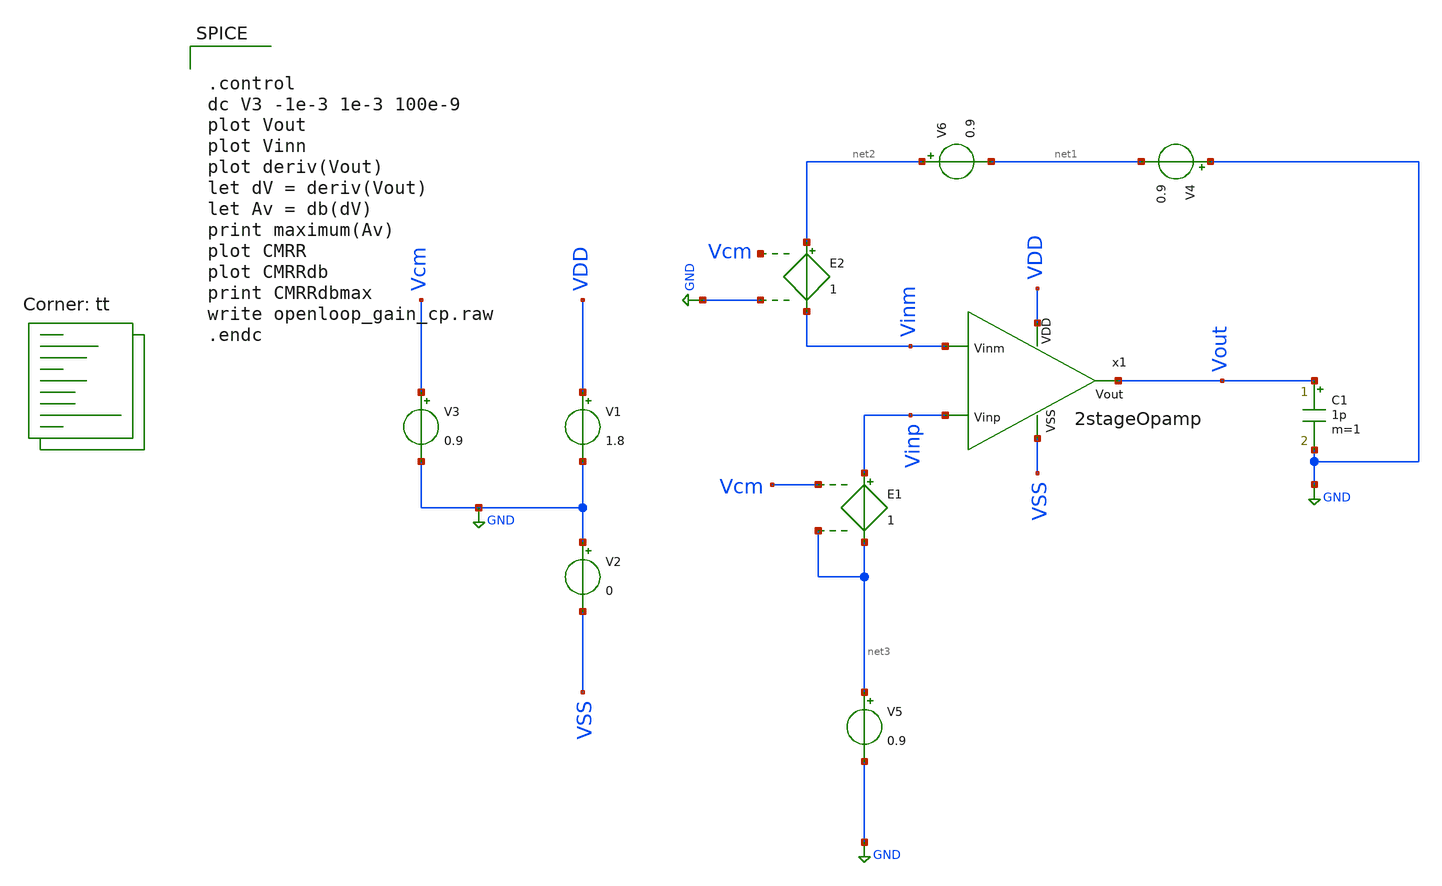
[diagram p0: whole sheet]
** sch_path: xschem/test/xschem/dec24_2stage_tbs/openloop_gain_cp.sch
**.subckt openloop_gain_cp
V1 VDD GND 1.8
V2 GND VSS 0
V3 Vcm GND 0.9
x1 VDD Vinm Vinp Vout VSS 2stageOpamp
E1 Vinp net3 Vcm net3 1
E2 net2 Vinm Vcm GND 1
V4 GND net1 0.9
C1 Vout GND 1p m=1
V5 net3 GND 0.9
V6 net2 net1 0.9
**** begin user architecture code


.control
dc V3 -1e-3 1e-3 100e-9
plot Vout
plot Vinn
plot deriv(Vout)
let dV = deriv(Vout)
let Av = db(dV)
print maximum(Av)
plot CMRR
plot CMRRdb
print CMRRdbmax
write openloop_gain_cp.raw
.endc



.lib $::SKYWATER_MODELS/sky130.lib.spice tt
**** end user architecture code
**.ends

* expanding   symbol:  amplifiers/dec24/2stageOpamp.sym # of pins=5
** sym_path: amplifiers/dec24/2stageOpamp.sym
** sch_path: amplifiers/dec24/2stageOpamp.sch
.subckt 2stageOpamp VDD Vinm Vinp Vout VSS
*.ipin Vinm
*.ipin Vinp
*.opin Vout
*.ipin VSS
*.ipin VDD
XM8 Vout net1 VSS VSS sky130_fd_pr__nfet_01v8 L=1 W=6 nf=1 ad='int((nf+1)/2) * W/nf * 0.29' as='int((nf+2)/2) * W/nf * 0.29'
+ pd='2*int((nf+1)/2) * (W/nf + 0.29)' ps='2*int((nf+2)/2) * (W/nf + 0.29)' nrd='0.29 / W' nrs='0.29 / W'
+ sa=0 sb=0 sd=0 mult=8 m=8
XM2 Vout Vb1 VDD VDD sky130_fd_pr__pfet_01v8_lvt L=1 W=9 nf=1 ad='int((nf+1)/2) * W/nf * 0.29' as='int((nf+2)/2) * W/nf * 0.29'
+ pd='2*int((nf+1)/2) * (W/nf + 0.29)' ps='2*int((nf+2)/2) * (W/nf + 0.29)' nrd='0.29 / W' nrs='0.29 / W'
+ sa=0 sb=0 sd=0 mult=3 m=3
XM5 net5 Vb3 net6 VSS sky130_fd_pr__nfet_01v8 L=1 W=4 nf=1 ad='int((nf+1)/2) * W/nf * 0.29' as='int((nf+2)/2) * W/nf * 0.29'
+ pd='2*int((nf+1)/2) * (W/nf + 0.29)' ps='2*int((nf+2)/2) * (W/nf + 0.29)' nrd='0.29 / W' nrs='0.29 / W'
+ sa=0 sb=0 sd=0 mult=3 m=3
XM17 net1 Vb3 net7 VSS sky130_fd_pr__nfet_01v8 L=1 W=4 nf=1 ad='int((nf+1)/2) * W/nf * 0.29' as='int((nf+2)/2) * W/nf * 0.29'
+ pd='2*int((nf+1)/2) * (W/nf + 0.29)' ps='2*int((nf+2)/2) * (W/nf + 0.29)' nrd='0.29 / W' nrs='0.29 / W'
+ sa=0 sb=0 sd=0 mult=3 m=3
XM3 net6 net5 VSS VSS sky130_fd_pr__nfet_01v8 L=1 W=8 nf=1 ad='int((nf+1)/2) * W/nf * 0.29' as='int((nf+2)/2) * W/nf * 0.29'
+ pd='2*int((nf+1)/2) * (W/nf + 0.29)' ps='2*int((nf+2)/2) * (W/nf + 0.29)' nrd='0.29 / W' nrs='0.29 / W'
+ sa=0 sb=0 sd=0 mult=1 m=1
XM19 net7 net5 VSS VSS sky130_fd_pr__nfet_01v8 L=1 W=8 nf=1 ad='int((nf+1)/2) * W/nf * 0.29' as='int((nf+2)/2) * W/nf * 0.29'
+ pd='2*int((nf+1)/2) * (W/nf + 0.29)' ps='2*int((nf+2)/2) * (W/nf + 0.29)' nrd='0.29 / W' nrs='0.29 / W'
+ sa=0 sb=0 sd=0 mult=1 m=1
V1 Vb1 GND 1.1
V2 Vb2 GND 0.7
V3 Vb3 GND 0.9
XM11 net8 Vb1 VDD VDD sky130_fd_pr__pfet_01v8_lvt L=1 W=9 nf=1 ad='int((nf+1)/2) * W/nf * 0.29' as='int((nf+2)/2) * W/nf * 0.29'
+ pd='2*int((nf+1)/2) * (W/nf + 0.29)' ps='2*int((nf+2)/2) * (W/nf + 0.29)' nrd='0.29 / W' nrs='0.29 / W'
+ sa=0 sb=0 sd=0 mult=2 m=2
XM1 net6 Vinm net8 VDD sky130_fd_pr__pfet_01v8_lvt L=1 W=8 nf=1 ad='int((nf+1)/2) * W/nf * 0.29' as='int((nf+2)/2) * W/nf * 0.29'
+ pd='2*int((nf+1)/2) * (W/nf + 0.29)' ps='2*int((nf+2)/2) * (W/nf + 0.29)' nrd='0.29 / W' nrs='0.29 / W'
+ sa=0 sb=0 sd=0 mult=3 m=3
XM15 net7 Vinp net8 VDD sky130_fd_pr__pfet_01v8_lvt L=1 W=8 nf=1 ad='int((nf+1)/2) * W/nf * 0.29' as='int((nf+2)/2) * W/nf * 0.29'
+ pd='2*int((nf+1)/2) * (W/nf + 0.29)' ps='2*int((nf+2)/2) * (W/nf + 0.29)' nrd='0.29 / W' nrs='0.29 / W'
+ sa=0 sb=0 sd=0 mult=3 m=3
XM7 net3 Vb1 VDD VDD sky130_fd_pr__pfet_01v8_lvt L=1 W=9 nf=1 ad='int((nf+1)/2) * W/nf * 0.29' as='int((nf+2)/2) * W/nf * 0.29'
+ pd='2*int((nf+1)/2) * (W/nf + 0.29)' ps='2*int((nf+2)/2) * (W/nf + 0.29)' nrd='0.29 / W' nrs='0.29 / W'
+ sa=0 sb=0 sd=0 mult=1 m=1
XM21 net4 Vb1 VDD VDD sky130_fd_pr__pfet_01v8_lvt L=1 W=9 nf=1 ad='int((nf+1)/2) * W/nf * 0.29' as='int((nf+2)/2) * W/nf * 0.29'
+ pd='2*int((nf+1)/2) * (W/nf + 0.29)' ps='2*int((nf+2)/2) * (W/nf + 0.29)' nrd='0.29 / W' nrs='0.29 / W'
+ sa=0 sb=0 sd=0 mult=1 m=1
XM9 net5 Vb2 net3 VDD sky130_fd_pr__pfet_01v8_lvt L=1 W=9 nf=1 ad='int((nf+1)/2) * W/nf * 0.29' as='int((nf+2)/2) * W/nf * 0.29'
+ pd='2*int((nf+1)/2) * (W/nf + 0.29)' ps='2*int((nf+2)/2) * (W/nf + 0.29)' nrd='0.29 / W' nrs='0.29 / W'
+ sa=0 sb=0 sd=0 mult=1 m=1
XM23 net1 Vb2 net4 VDD sky130_fd_pr__pfet_01v8_lvt L=1 W=9 nf=1 ad='int((nf+1)/2) * W/nf * 0.29' as='int((nf+2)/2) * W/nf * 0.29'
+ pd='2*int((nf+1)/2) * (W/nf + 0.29)' ps='2*int((nf+2)/2) * (W/nf + 0.29)' nrd='0.29 / W' nrs='0.29 / W'
+ sa=0 sb=0 sd=0 mult=1 m=1
XC4 net2 Vout sky130_fd_pr__cap_mim_m3_2 W=7 L=7 MF=4 m=4
R4 net1 net2 7k m=1
.ends

.GLOBAL GND
.end
